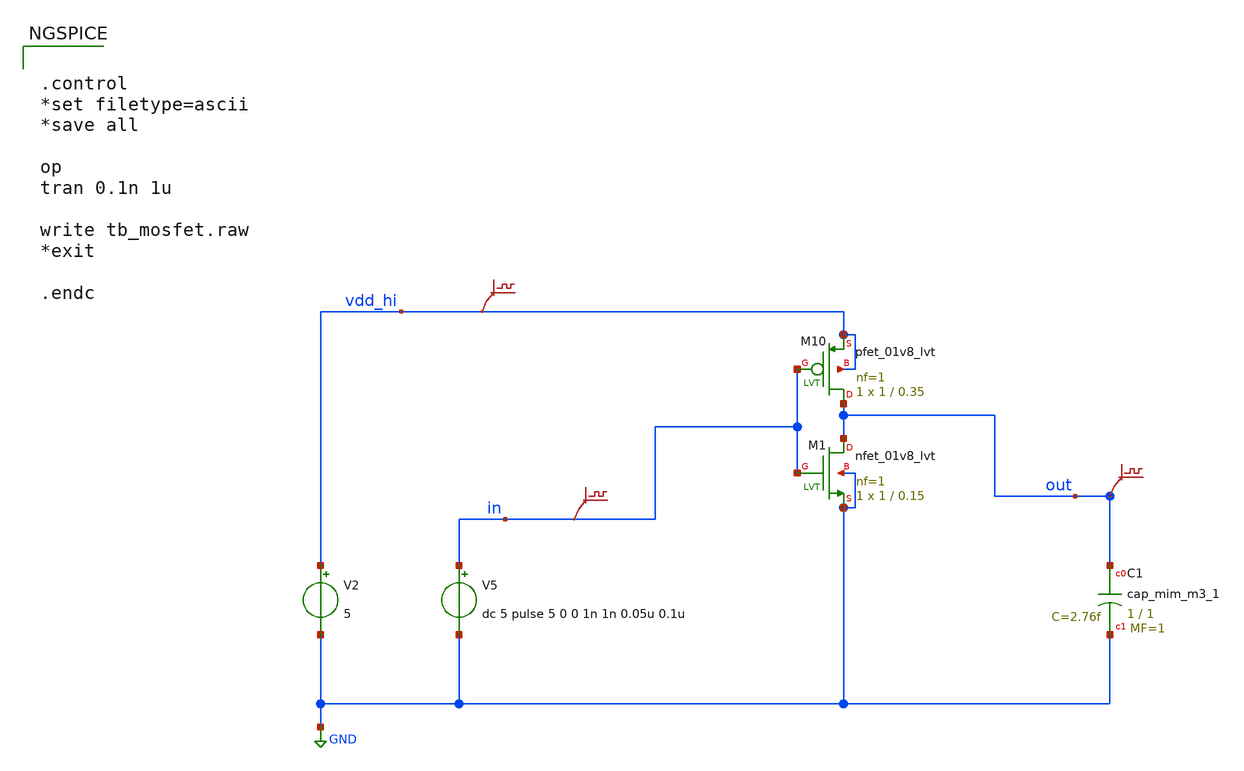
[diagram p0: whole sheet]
** sch_path: custom_gds/tt_um_test_commit/xschem/inverter_tb.sch
**.subckt inverter_tb
V2 vdd_hi GND 5
V5 in GND dc 5 pulse 5 0 0 1n 1n 0.05u 0.1u
.save v(vdd_hi)
.save v(in)
.save v(out)
XM10 out in vdd_hi vdd_hi sky130_fd_pr__pfet_01v8_lvt L=0.35 W=1 nf=1 ad='int((1 + 1)/2) * 1 / 1 * 0.29'
+ as='int((1 + 2)/2) * 1 / 1 * 0.29' pd='2*int((1 + 1)/2) * (1 / 1 + 0.29)' ps='2*int((1 + 2)/2) * (1 / 1 + 0.29)'
+ nrd='0.29 / 1 ' nrs='0.29 / 1 ' sa=0 sb=0 sd=0 mult=1 m=1
XM1 out in GND GND sky130_fd_pr__nfet_01v8_lvt L=0.15 W=1 nf=1 ad='int((1 + 1)/2) * 1 / 1 * 0.29' as='int((1 + 2)/2) * 1 / 1 * 0.29'
+ pd='2*int((1 + 1)/2) * (1 / 1 + 0.29)' ps='2*int((1 + 2)/2) * (1 / 1 + 0.29)' nrd='0.29 / 1 ' nrs='0.29 / 1 '
+ sa=0 sb=0 sd=0 mult=1 m=1
XC1 out GND sky130_fd_pr__cap_mim_m3_1 W=1 L=1 MF=1 m=1
**** begin user architecture code


.control
*set filetype=ascii
*save all

op
tran 0.1n 1u

write tb_mosfet.raw
*exit

.endc



** opencircuitdesign pdks install
.lib $::SKYWATER_MODELS/sky130.lib.spice tt


**** end user architecture code
**.ends
.GLOBAL GND
.end
